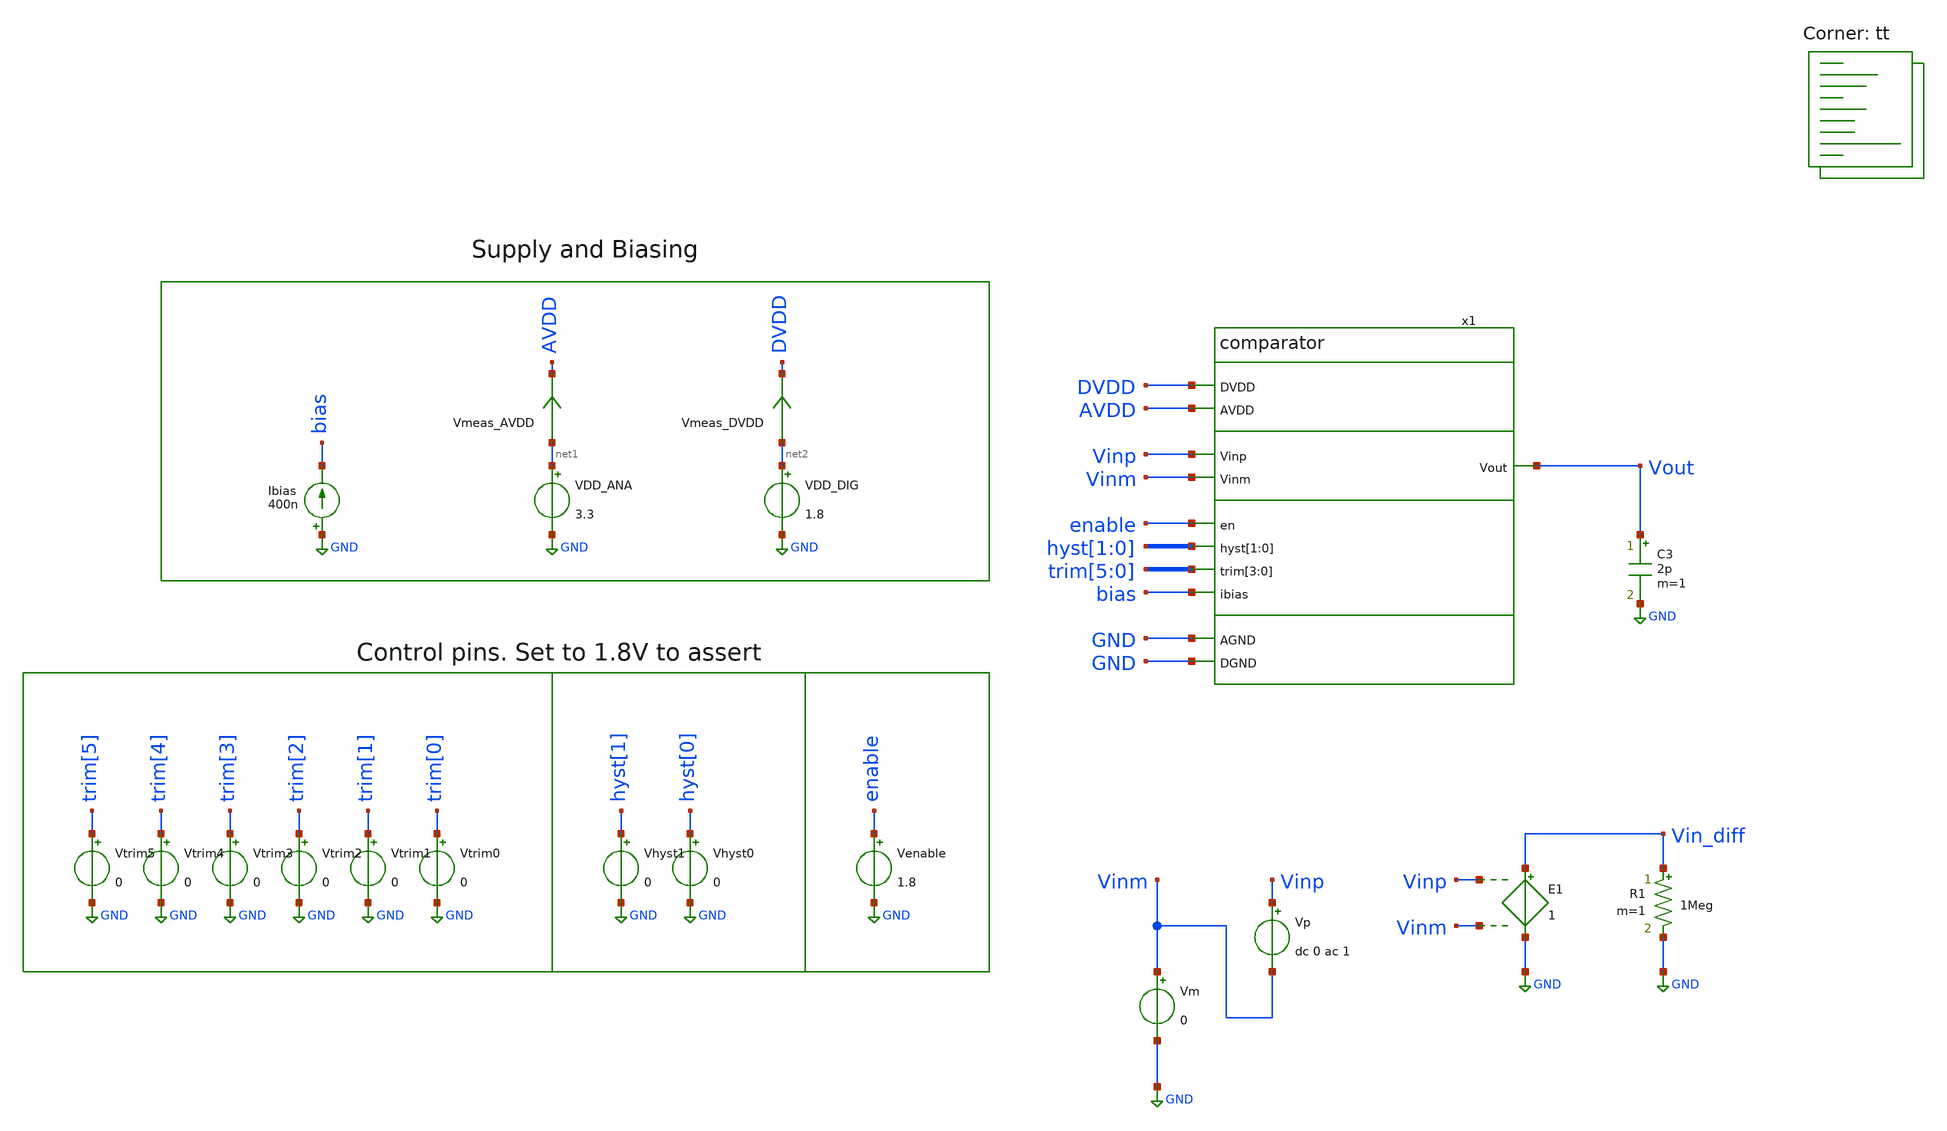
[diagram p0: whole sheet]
** sch_path: xschem/tb_comparator_capacitance.sch
**.subckt tb_comparator_capacitance
Vp Vinp Vinm dc 0 ac 1
VDD_ANA net1 GND 3.3
VDD_DIG net2 GND 1.8
Ibias GND bias 400n
C3 Vout GND 2p m=1
Vm Vinm GND 0
Vmeas_AVDD net1 AVDD 0
.save i(vmeas_avdd)
Vmeas_DVDD net2 DVDD 0
.save i(vmeas_dvdd)
E1 Vin_diff GND Vinp Vinm 1
Vtrim3 trim[3] GND 0
Vtrim2 trim[2] GND 0
Vtrim1 trim[1] GND 0
Vtrim0 trim[0] GND 0
Vhyst1 hyst[1] GND 0
Vhyst0 hyst[0] GND 0
Venable enable GND 1.8
Vtrim5 trim[5] GND 0
Vtrim4 trim[4] GND 0
R1 Vin_diff GND 1Meg m=1
x1 DVDD AVDD GND GND Vinp Vout Vinm enable hyst[1] hyst[0] trim[5] trim[4] trim[3] trim[2] bias
+ comparator
**** begin user architecture code
.lib $::SKYWATER_MODELS/sky130.lib.spice tt


.save all
.savecurrents
.ac dec 51 200 20k

.control
let vec=unitvec(1)
set plotstr=' '
foreach temp_val -40 27 85
   set temp=$temp_val
   foreach vdd_ana_val 2.95 3.3 5.5
      alter VDD_ANA $vdd_ana_val
      foreach vm_val 0 {$vdd_ana_val/4} {$vdd_ana_val/2} {$vdd_ana_val*3/4} {-0.1+$vdd_ana_val}
         alter Vm $vm_val
         foreach ibias_val 400n
            alter Ibias $ibias_val
            run
            let cap = -imag(i(vp))/real(v(vinp))/2/3.14159/frequency
            let cap_max = vecmax(cap)
            set filetype=ascii
            set appendwrite
            set wr_singlescale
            setscale vec
            wrdata results_capacitance.out cap_max
         end
      end
   end
end
*setscale frequency
*plot $plotstr
.endc


**** end user architecture code
**.ends
.GLOBAL GND
.end
